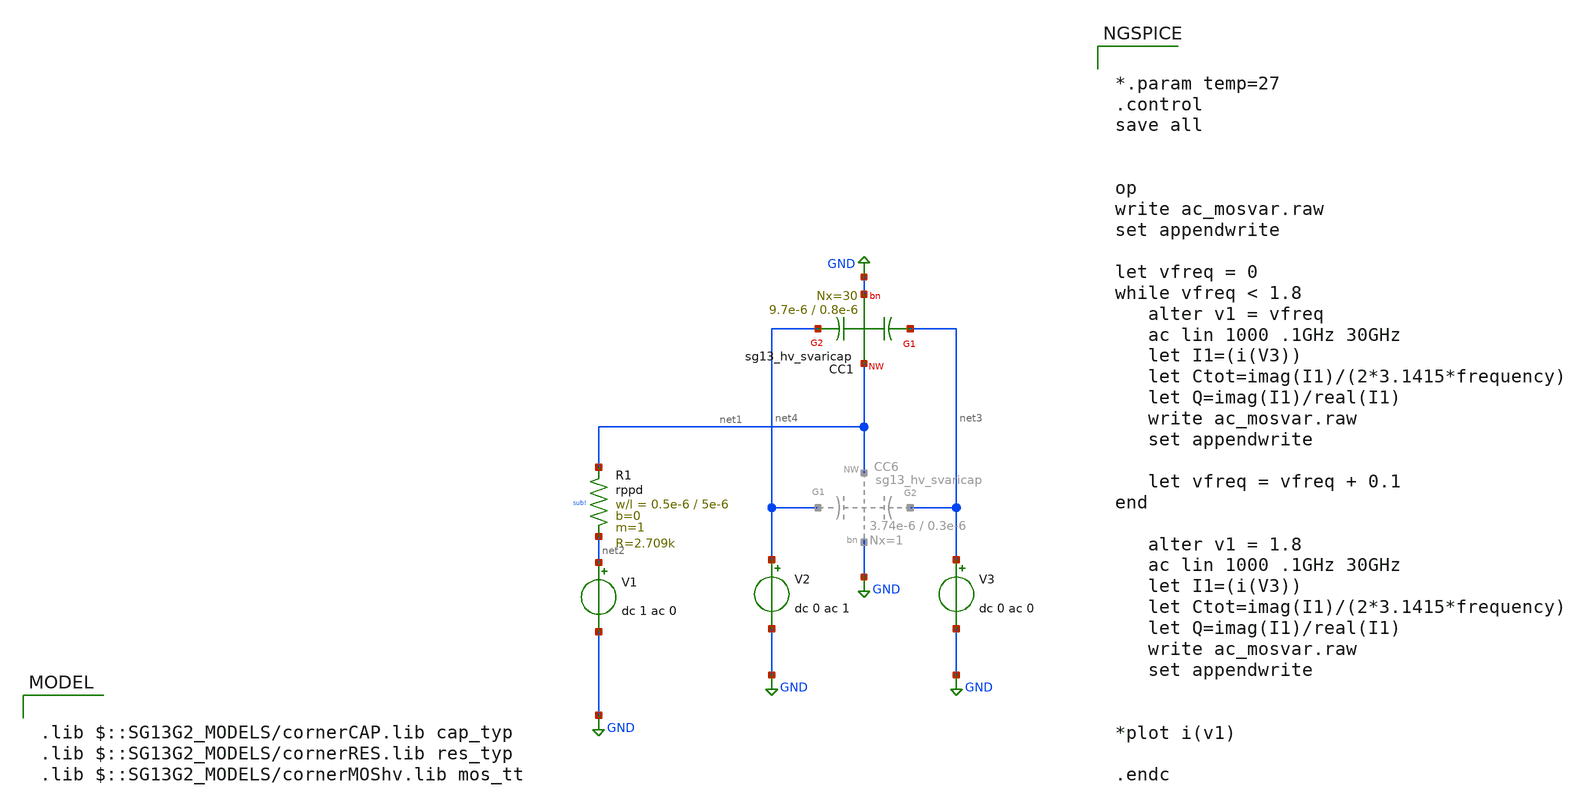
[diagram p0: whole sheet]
** sch_path: design_data/xschem/measuremenst_and_test_of_idas/ac_svaricap_test2_x30.sch
**.subckt ac_svaricap_test2_x30
V1 net2 GND dc 1 ac 0
V3 net3 GND dc 0 ac 0
V2 net4 GND dc 0 ac 1
XC1 net3 net1 net4 GND sg13_hv_svaricap w=9.7e-6 l=0.8e-6 Nx=30
XR1 net1 net2 sub! rppd w=0.5e-6 l=5e-6 m=1 b=0 mm_ok=1
**** begin user architecture code

.lib $::SG13G2_MODELS/cornerCAP.lib cap_typ
.lib $::SG13G2_MODELS/cornerRES.lib res_typ
.lib $::SG13G2_MODELS/cornerMOShv.lib mos_tt



*.param temp=27
.control
save all


op
write ac_mosvar.raw
set appendwrite

let vfreq = 0
while vfreq < 1.8
   alter v1 = vfreq
   ac lin 1000 .1GHz 30GHz
   let I1=(i(V3))
   let Ctot=imag(I1)/(2*3.1415*frequency)
   let Q=imag(I1)/real(I1)
   write ac_mosvar.raw
   set appendwrite

   let vfreq = vfreq + 0.1
end

   alter v1 = 1.8
   ac lin 1000 .1GHz 30GHz
   let I1=(i(V3))
   let Ctot=imag(I1)/(2*3.1415*frequency)
   let Q=imag(I1)/real(I1)
   write ac_mosvar.raw
   set appendwrite


*plot i(v1)

.endc


**** end user architecture code
**.ends
.GLOBAL GND
.end
